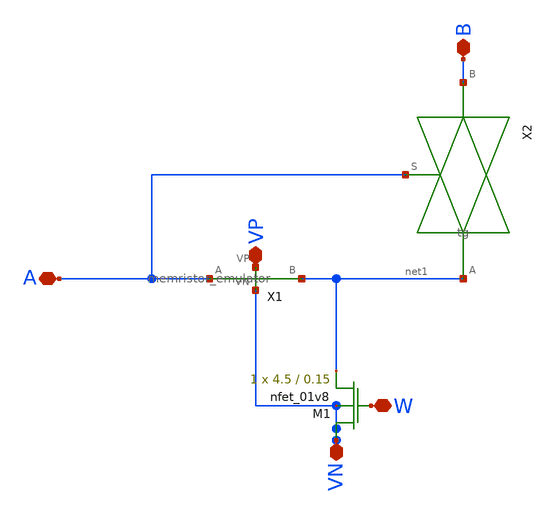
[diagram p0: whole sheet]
** sch_path: schematic/res.sch
**.subckt res A W B VP VN
*.iopin A
*.iopin W
*.iopin B
*.iopin VP
*.iopin VN
XM1 VN W net1 VN sky130_fd_pr__nfet_01v8 L=0.15 W=4.5 nf=1 ad='int((nf+1)/2) * W/nf * 0.29' as='int((nf+2)/2) * W/nf * 0.29'
+ pd='2*int((nf+1)/2) * (W/nf + 0.29)' ps='2*int((nf+2)/2) * (W/nf + 0.29)' nrd='0.29 / W' nrs='0.29 / W'
+ sa=0 sb=0 sd=0 mult=1 m=1
X1 VP VN net1 A memristor_emulator
X2 A net1 B tg
**.ends

* expanding   symbol:
*+  /home/madvlsi/Documents/second/neuromorphic_computing_final/schematic/memristor_emulator.sym # of pins=4
** sym_path: schematic/memristor_emulator.sym
** sch_path: schematic/memristor_emulator.sch
.subckt memristor_emulator VP VN B A
*.ipin A
*.iopin VN
*.iopin VP
*.opin B
XM1 B in_cap A B sky130_fd_pr__pfet_01v8 L=0.3 W=12 nf=1 ad='int((nf+1)/2) * W/nf * 0.29' as='int((nf+2)/2) * W/nf * 0.29'
+ pd='2*int((nf+1)/2) * (W/nf + 0.29)' ps='2*int((nf+2)/2) * (W/nf + 0.29)' nrd='0.29 / W' nrs='0.29 / W'
+ sa=0 sb=0 sd=0 mult=1 m=1
XM2 VP A in_cap VP sky130_fd_pr__pfet_01v8 L=2 W=3 nf=1 ad='int((nf+1)/2) * W/nf * 0.29' as='int((nf+2)/2) * W/nf * 0.29'
+ pd='2*int((nf+1)/2) * (W/nf + 0.29)' ps='2*int((nf+2)/2) * (W/nf + 0.29)' nrd='0.29 / W' nrs='0.29 / W'
+ sa=0 sb=0 sd=0 mult=1 m=1
XM3 VN in_cap VN VN sky130_fd_pr__nfet_01v8 L=20 W=20 nf=1 ad='int((nf+1)/2) * W/nf * 0.29' as='int((nf+2)/2) * W/nf * 0.29'
+ pd='2*int((nf+1)/2) * (W/nf + 0.29)' ps='2*int((nf+2)/2) * (W/nf + 0.29)' nrd='0.29 / W' nrs='0.29 / W'
+ sa=0 sb=0 sd=0 mult=1 m=1
XM4 VN B in_cap VN sky130_fd_pr__nfet_01v8 L=3 W=2 nf=1 ad='int((nf+1)/2) * W/nf * 0.29' as='int((nf+2)/2) * W/nf * 0.29'
+ pd='2*int((nf+1)/2) * (W/nf + 0.29)' ps='2*int((nf+2)/2) * (W/nf + 0.29)' nrd='0.29 / W' nrs='0.29 / W'
+ sa=0 sb=0 sd=0 mult=1 m=1
.ends


* expanding   symbol:  /home/madvlsi/Documents/second/neuromorphic_computing_final/schematic/tg.sym
*+ # of pins=3
** sym_path: schematic/tg.sym
** sch_path: schematic/tg.sch
.subckt tg S A B
*.ipin S
*.iopin B
*.iopin A
XM1 B net1 A VDD sky130_fd_pr__pfet_01v8 L=0.3 W=6 nf=1 ad='int((nf+1)/2) * W/nf * 0.29' as='int((nf+2)/2) * W/nf * 0.29'
+ pd='2*int((nf+1)/2) * (W/nf + 0.29)' ps='2*int((nf+2)/2) * (W/nf + 0.29)' nrd='0.29 / W' nrs='0.29 / W'
+ sa=0 sb=0 sd=0 mult=1 m=1
XM2 B S A GND sky130_fd_pr__nfet_01v8 L=0.3 W=6 nf=1 ad='int((nf+1)/2) * W/nf * 0.29' as='int((nf+2)/2) * W/nf * 0.29'
+ pd='2*int((nf+1)/2) * (W/nf + 0.29)' ps='2*int((nf+2)/2) * (W/nf + 0.29)' nrd='0.29 / W' nrs='0.29 / W'
+ sa=0 sb=0 sd=0 mult=1 m=1
X1 S GND VDD net1 inverter
.ends


* expanding   symbol:
*+  /home/madvlsi/Documents/second/neuromorphic_computing_final/schematic/inverter.sym # of pins=4
** sym_path: schematic/inverter.sym
** sch_path: schematic/inverter.sch
.subckt inverter A VN VP Y
*.ipin A
*.iopin VP
*.iopin VN
*.opin Y
XM1 Y A VN VN sky130_fd_pr__nfet_01v8 L=0.15 W=1 nf=1 ad='int((nf+1)/2) * W/nf * 0.29' as='int((nf+2)/2) * W/nf * 0.29'
+ pd='2*int((nf+1)/2) * (W/nf + 0.29)' ps='2*int((nf+2)/2) * (W/nf + 0.29)' nrd='0.29 / W' nrs='0.29 / W'
+ sa=0 sb=0 sd=0 mult=1 m=1
XM2 Y A VP VP sky130_fd_pr__pfet_01v8 L=0.15 W=1 nf=1 ad='int((nf+1)/2) * W/nf * 0.29' as='int((nf+2)/2) * W/nf * 0.29'
+ pd='2*int((nf+1)/2) * (W/nf + 0.29)' ps='2*int((nf+2)/2) * (W/nf + 0.29)' nrd='0.29 / W' nrs='0.29 / W'
+ sa=0 sb=0 sd=0 mult=1 m=1
.ends

.GLOBAL VDD
.GLOBAL GND
.end
